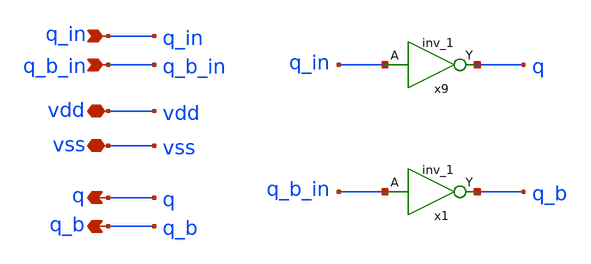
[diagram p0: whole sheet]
** sch_path: xschem/comparator/comparator_buff.sch
**.subckt comparator_buff q q_b vdd vss q_b_in q_in
*.opin q
*.opin q_b
*.iopin vdd
*.iopin vss
*.ipin q_b_in
*.ipin q_in
x9 q_in vss vss vdd vdd q sky130_fd_sc_hd__inv_1
x1 q_b_in vss vss vdd vdd q_b sky130_fd_sc_hd__inv_1
**.ends
.end
